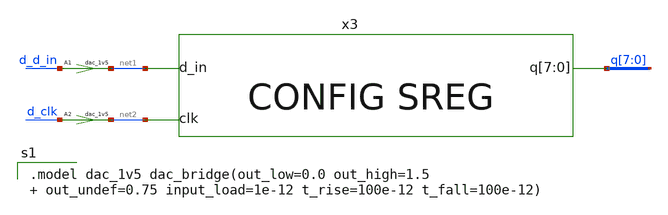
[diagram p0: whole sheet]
** sch_path: xschem/cfg_shift_register_tb.sch
**.subckt cfg_shift_register_tb
x3 net2 net1 q[7] q[6] q[5] q[4] q[3] q[2] q[1] q[0] VDD GND cfg_shift_register
A1 [ d_d_in ] [ net1 ] dac_1v5
A2 [ d_clk ] [ net2 ] dac_1v5
**** begin user architecture code

.model dac_1v5 dac_bridge(out_low=0.0 out_high=1.5   out_undef=0.75 input_load=1e-12 t_rise=100e-12
+ t_fall=100e-12)

 ** Local library links to pdk
.lib sky130/libs/tt_lib.spice tt
.include $::SKYWATER_STDCELLS/sky130_fd_sc_hd.spice

**** end user architecture code
**.ends

* expanding   symbol:  xschem/cfg_shift_register.sym # of pins=3
** sym_path: xschem/cfg_shift_register.sym
** sch_path: xschem/cfg_shift_register.sch
.subckt cfg_shift_register clk d_in q[7] q[6] q[5] q[4] q[3] q[2] q[1] q[0] VDD GND
*.ipin clk
*.ipin d_in
*.opin q[7],q[6],q[5],q[4],q[3],q[2],q[1],q[0]
x1 clk d_in GND GND VDD VDD q[0] sky130_fd_sc_hd__dfxtp_1
x2 clk q[0] GND GND VDD VDD q[1] sky130_fd_sc_hd__dfxtp_1
x3 clk q[1] GND GND VDD VDD q[2] sky130_fd_sc_hd__dfxtp_1
x4 clk q[2] GND GND VDD VDD q[3] sky130_fd_sc_hd__dfxtp_1
x5 clk q[3] GND GND VDD VDD q[4] sky130_fd_sc_hd__dfxtp_1
x6 clk q[4] GND GND VDD VDD q[5] sky130_fd_sc_hd__dfxtp_1
x7 clk q[5] GND GND VDD VDD q[6] sky130_fd_sc_hd__dfxtp_1
x8 clk q[6] GND GND VDD VDD q[7] sky130_fd_sc_hd__dfxtp_1
.ends

**** begin user architecture code


* power voltage
vvdd VDD 0 1.5

** STATIC CONTOL


** Signal
a_source [d_clk d_d_in] d_source1
.model d_source1 d_source(input_file="cfg_sreg_din.txt")


.control
save all
set temp=27

* RUN SIMULATION
tran 1n 20n

* OUTPUT
set hcopydevtype = svg
hardcopy ./sreg_tb.svg  net1-2 net2-2 "q[0]" "q[1]"+2 "q[2]"+4 "q[3]"+6 "q[4]"+8 "q[5]"+10 "q[6]"+12
+ "q[7]"+14 title 'SSTL Test Circuit'

.endc


**** end user architecture code
.end
